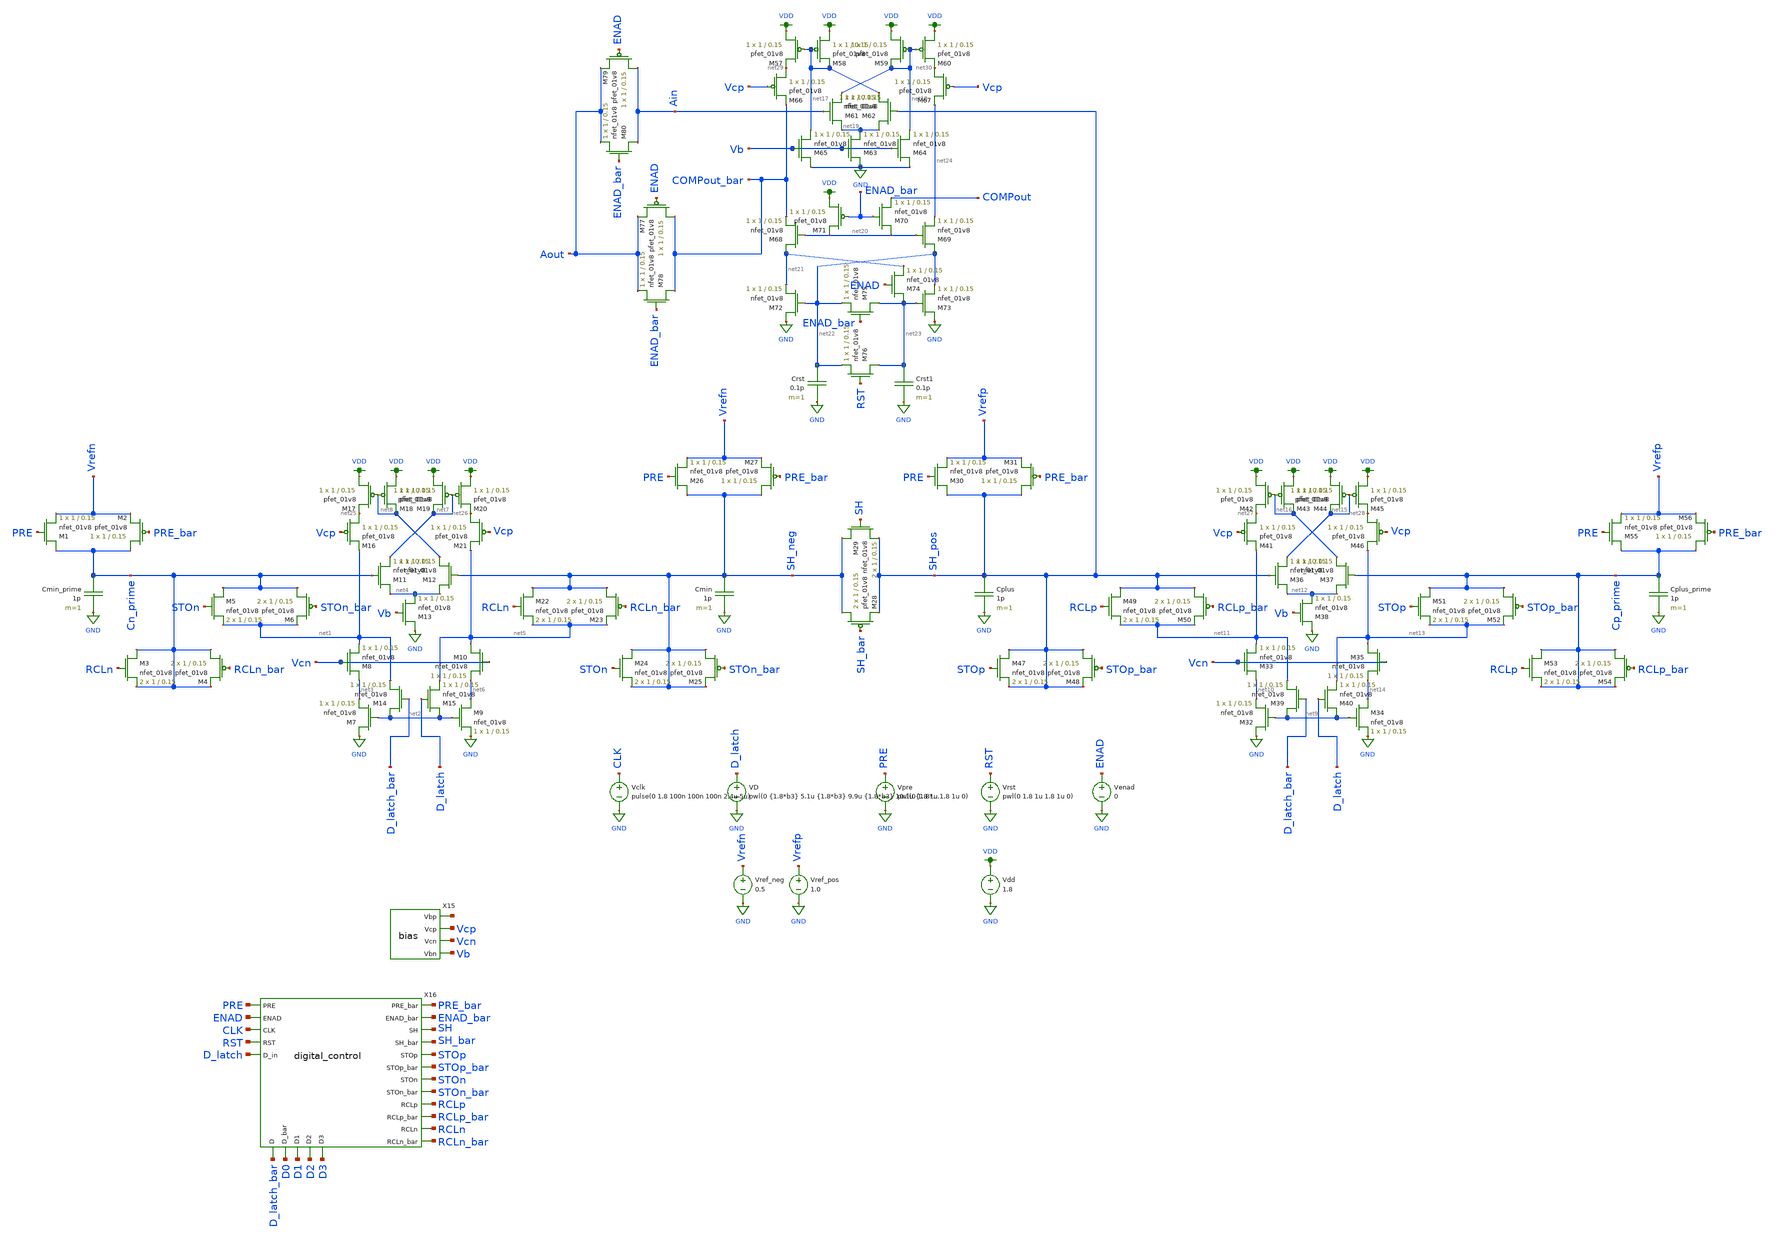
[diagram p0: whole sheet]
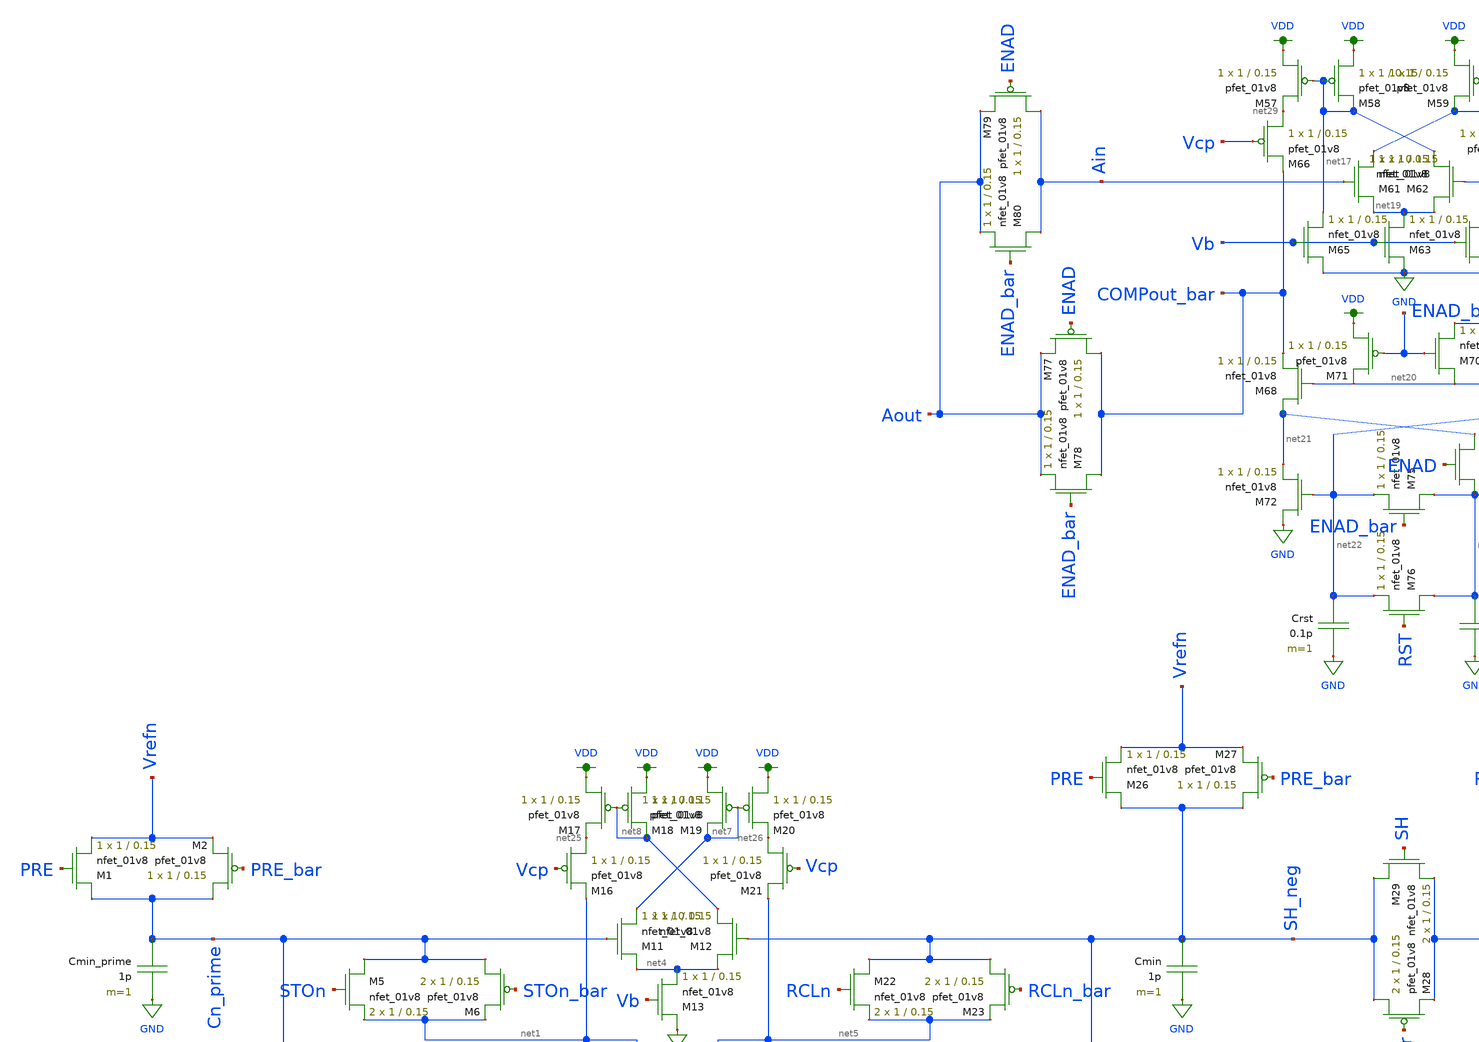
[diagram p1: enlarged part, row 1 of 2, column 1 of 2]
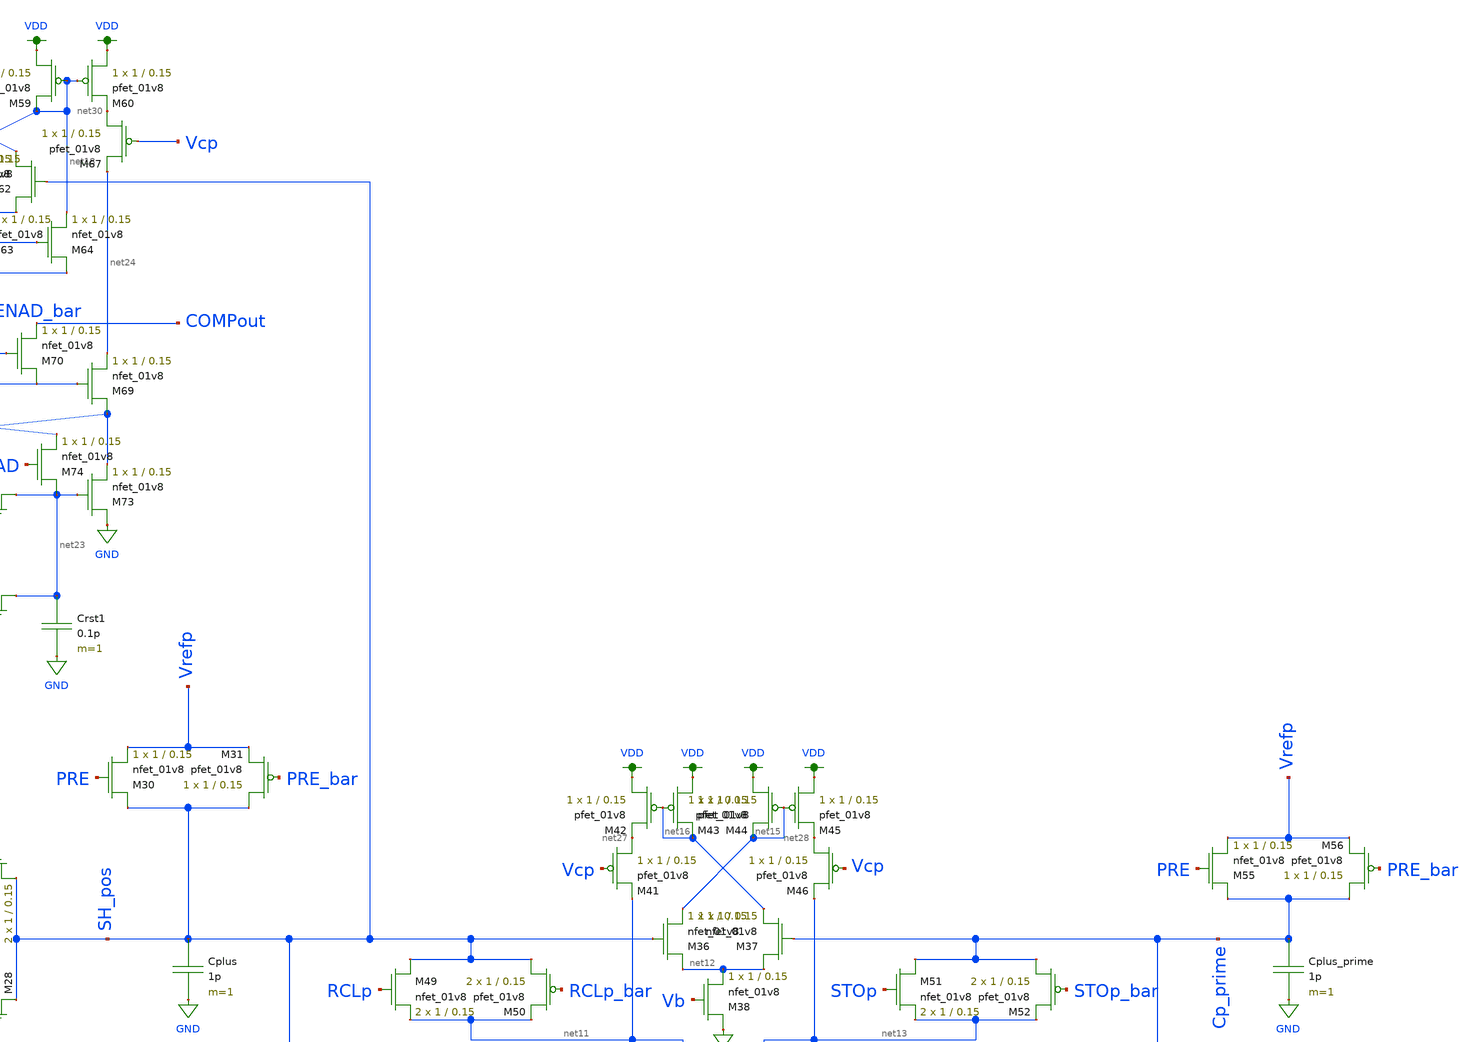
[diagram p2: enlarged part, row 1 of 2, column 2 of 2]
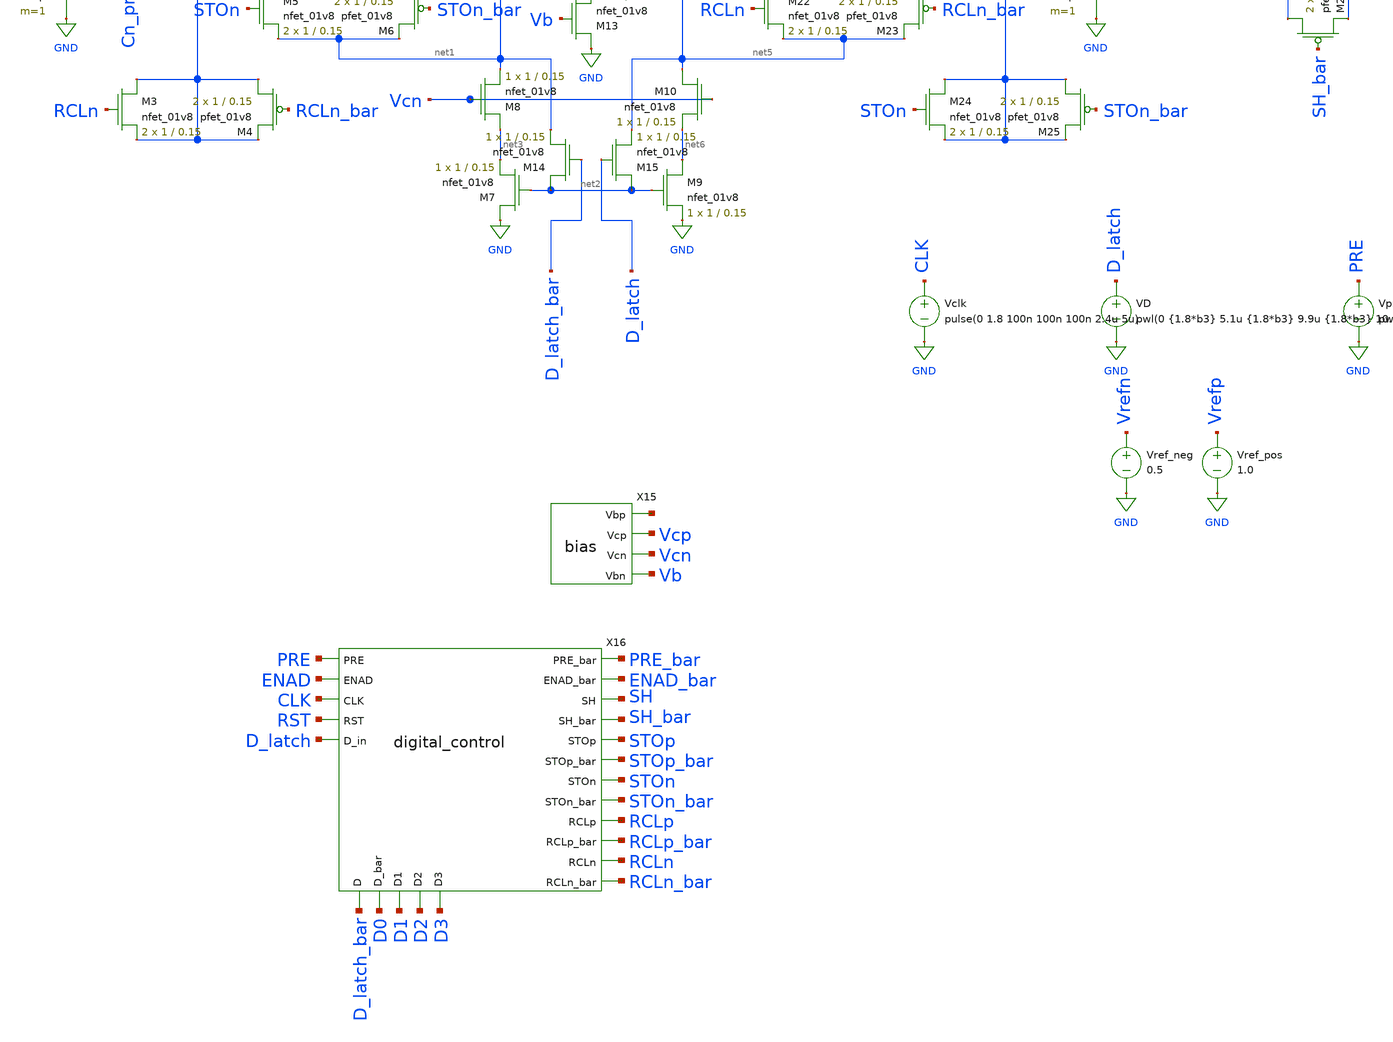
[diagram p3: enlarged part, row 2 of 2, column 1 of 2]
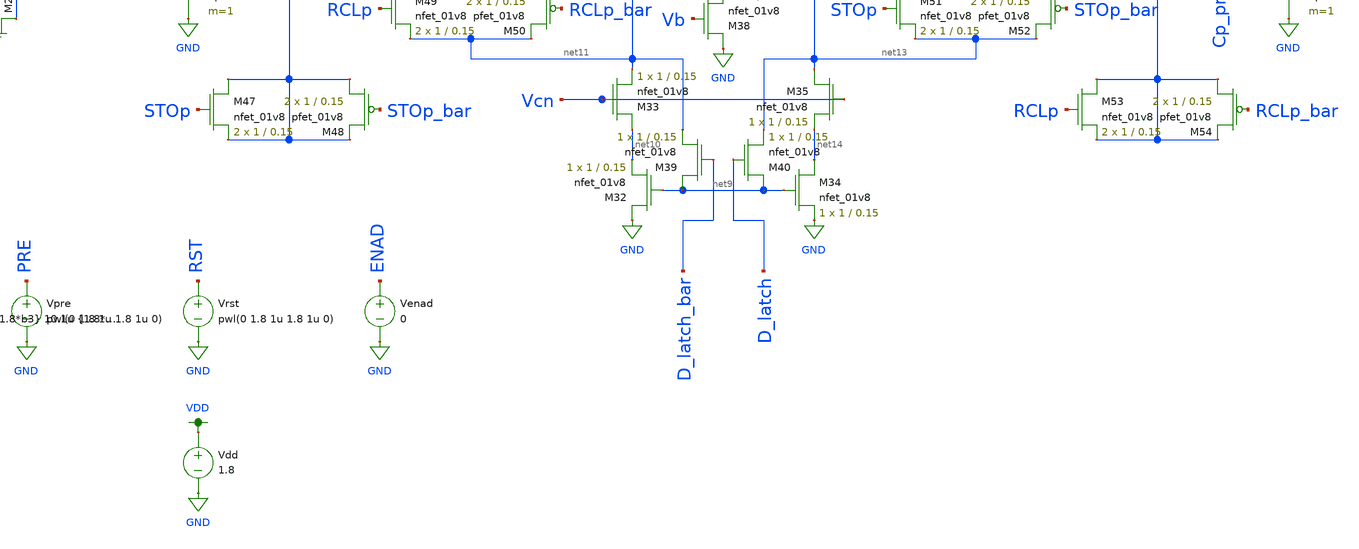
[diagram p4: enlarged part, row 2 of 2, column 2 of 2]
** sch_path: simulations/test_harness_dac.sch
**.subckt test_harness_dac
XM1 Cn_prime PRE Vrefn GND sky130_fd_pr__nfet_01v8 L=0.15 W=1 nf=1 ad='int((nf+1)/2) * W/nf * 0.29' as='int((nf+2)/2) * W/nf * 0.29'
+ pd='2*int((nf+1)/2) * (W/nf + 0.29)' ps='2*int((nf+2)/2) * (W/nf + 0.29)' nrd='0.29 / W' nrs='0.29 / W'
+ sa=0 sb=0 sd=0 mult=1 m=1
XM2 Cn_prime PRE_bar Vrefn VDD sky130_fd_pr__pfet_01v8 L=0.15 W=1 nf=1 ad='int((nf+1)/2) * W/nf * 0.29'
+ as='int((nf+2)/2) * W/nf * 0.29' pd='2*int((nf+1)/2) * (W/nf + 0.29)' ps='2*int((nf+2)/2) * (W/nf + 0.29)'
+ nrd='0.29 / W' nrs='0.29 / W' sa=0 sb=0 sd=0 mult=1 m=1
Cmin_prime Cn_prime GND 1p m=1
XM3 Cn_prime RCLn Cn_prime GND sky130_fd_pr__nfet_01v8 L=0.15 W=1 nf=1 ad='int((nf+1)/2) * W/nf * 0.29'
+ as='int((nf+2)/2) * W/nf * 0.29' pd='2*int((nf+1)/2) * (W/nf + 0.29)' ps='2*int((nf+2)/2) * (W/nf + 0.29)'
+ nrd='0.29 / W' nrs='0.29 / W' sa=0 sb=0 sd=0 mult=2 m=2
XM4 Cn_prime RCLn_bar Cn_prime VDD sky130_fd_pr__pfet_01v8 L=0.15 W=1 nf=1 ad='int((nf+1)/2) * W/nf * 0.29'
+ as='int((nf+2)/2) * W/nf * 0.29' pd='2*int((nf+1)/2) * (W/nf + 0.29)' ps='2*int((nf+2)/2) * (W/nf + 0.29)'
+ nrd='0.29 / W' nrs='0.29 / W' sa=0 sb=0 sd=0 mult=2 m=2
XM5 Cn_prime STOn net1 GND sky130_fd_pr__nfet_01v8 L=0.15 W=1 nf=1 ad='int((nf+1)/2) * W/nf * 0.29' as='int((nf+2)/2) * W/nf * 0.29'
+ pd='2*int((nf+1)/2) * (W/nf + 0.29)' ps='2*int((nf+2)/2) * (W/nf + 0.29)' nrd='0.29 / W' nrs='0.29 / W'
+ sa=0 sb=0 sd=0 mult=2 m=2
XM6 Cn_prime STOn_bar net1 VDD sky130_fd_pr__pfet_01v8 L=0.15 W=1 nf=1 ad='int((nf+1)/2) * W/nf * 0.29'
+ as='int((nf+2)/2) * W/nf * 0.29' pd='2*int((nf+1)/2) * (W/nf + 0.29)' ps='2*int((nf+2)/2) * (W/nf + 0.29)'
+ nrd='0.29 / W' nrs='0.29 / W' sa=0 sb=0 sd=0 mult=2 m=2
XM7 GND net2 net3 GND sky130_fd_pr__nfet_01v8 L=0.15 W=1 nf=1 ad='int((nf+1)/2) * W/nf * 0.29' as='int((nf+2)/2) * W/nf * 0.29'
+ pd='2*int((nf+1)/2) * (W/nf + 0.29)' ps='2*int((nf+2)/2) * (W/nf + 0.29)' nrd='0.29 / W' nrs='0.29 / W'
+ sa=0 sb=0 sd=0 mult=1 m=1
XM8 net3 Vcn net1 GND sky130_fd_pr__nfet_01v8 L=0.15 W=1 nf=1 ad='int((nf+1)/2) * W/nf * 0.29' as='int((nf+2)/2) * W/nf * 0.29'
+ pd='2*int((nf+1)/2) * (W/nf + 0.29)' ps='2*int((nf+2)/2) * (W/nf + 0.29)' nrd='0.29 / W' nrs='0.29 / W'
+ sa=0 sb=0 sd=0 mult=1 m=1
XM9 net6 net2 GND GND sky130_fd_pr__nfet_01v8 L=0.15 W=1 nf=1 ad='int((nf+1)/2) * W/nf * 0.29' as='int((nf+2)/2) * W/nf * 0.29'
+ pd='2*int((nf+1)/2) * (W/nf + 0.29)' ps='2*int((nf+2)/2) * (W/nf + 0.29)' nrd='0.29 / W' nrs='0.29 / W'
+ sa=0 sb=0 sd=0 mult=1 m=1
XM10 net5 Vcn net6 GND sky130_fd_pr__nfet_01v8 L=0.15 W=1 nf=1 ad='int((nf+1)/2) * W/nf * 0.29' as='int((nf+2)/2) * W/nf * 0.29'
+ pd='2*int((nf+1)/2) * (W/nf + 0.29)' ps='2*int((nf+2)/2) * (W/nf + 0.29)' nrd='0.29 / W' nrs='0.29 / W'
+ sa=0 sb=0 sd=0 mult=1 m=1
XM11 net4 Cn_prime net7 GND sky130_fd_pr__nfet_01v8 L=0.15 W=1 nf=1 ad='int((nf+1)/2) * W/nf * 0.29'
+ as='int((nf+2)/2) * W/nf * 0.29' pd='2*int((nf+1)/2) * (W/nf + 0.29)' ps='2*int((nf+2)/2) * (W/nf + 0.29)'
+ nrd='0.29 / W' nrs='0.29 / W' sa=0 sb=0 sd=0 mult=1 m=1
XM12 net4 SH_neg net8 GND sky130_fd_pr__nfet_01v8 L=0.15 W=1 nf=1 ad='int((nf+1)/2) * W/nf * 0.29' as='int((nf+2)/2) * W/nf * 0.29'
+ pd='2*int((nf+1)/2) * (W/nf + 0.29)' ps='2*int((nf+2)/2) * (W/nf + 0.29)' nrd='0.29 / W' nrs='0.29 / W'
+ sa=0 sb=0 sd=0 mult=1 m=1
XM13 GND Vb net4 GND sky130_fd_pr__nfet_01v8 L=0.15 W=1 nf=1 ad='int((nf+1)/2) * W/nf * 0.29' as='int((nf+2)/2) * W/nf * 0.29'
+ pd='2*int((nf+1)/2) * (W/nf + 0.29)' ps='2*int((nf+2)/2) * (W/nf + 0.29)' nrd='0.29 / W' nrs='0.29 / W'
+ sa=0 sb=0 sd=0 mult=1 m=1
XM14 net2 D_latch_bar net1 GND sky130_fd_pr__nfet_01v8 L=0.15 W=1 nf=1 ad='int((nf+1)/2) * W/nf * 0.29'
+ as='int((nf+2)/2) * W/nf * 0.29' pd='2*int((nf+1)/2) * (W/nf + 0.29)' ps='2*int((nf+2)/2) * (W/nf + 0.29)'
+ nrd='0.29 / W' nrs='0.29 / W' sa=0 sb=0 sd=0 mult=1 m=1
XM15 net2 D_latch net5 GND sky130_fd_pr__nfet_01v8 L=0.15 W=1 nf=1 ad='int((nf+1)/2) * W/nf * 0.29' as='int((nf+2)/2) * W/nf * 0.29'
+ pd='2*int((nf+1)/2) * (W/nf + 0.29)' ps='2*int((nf+2)/2) * (W/nf + 0.29)' nrd='0.29 / W' nrs='0.29 / W'
+ sa=0 sb=0 sd=0 mult=1 m=1
XM16 net25 Vcp net1 VDD sky130_fd_pr__pfet_01v8 L=0.15 W=1 nf=1 ad='int((nf+1)/2) * W/nf * 0.29' as='int((nf+2)/2) * W/nf * 0.29'
+ pd='2*int((nf+1)/2) * (W/nf + 0.29)' ps='2*int((nf+2)/2) * (W/nf + 0.29)' nrd='0.29 / W' nrs='0.29 / W'
+ sa=0 sb=0 sd=0 mult=1 m=1
XM17 VDD net8 net25 VDD sky130_fd_pr__pfet_01v8 L=0.15 W=1 nf=1 ad='int((nf+1)/2) * W/nf * 0.29' as='int((nf+2)/2) * W/nf * 0.29'
+ pd='2*int((nf+1)/2) * (W/nf + 0.29)' ps='2*int((nf+2)/2) * (W/nf + 0.29)' nrd='0.29 / W' nrs='0.29 / W'
+ sa=0 sb=0 sd=0 mult=1 m=1
XM18 VDD net8 net8 VDD sky130_fd_pr__pfet_01v8 L=0.15 W=1 nf=1 ad='int((nf+1)/2) * W/nf * 0.29' as='int((nf+2)/2) * W/nf * 0.29'
+ pd='2*int((nf+1)/2) * (W/nf + 0.29)' ps='2*int((nf+2)/2) * (W/nf + 0.29)' nrd='0.29 / W' nrs='0.29 / W'
+ sa=0 sb=0 sd=0 mult=1 m=1
XM19 VDD net7 net7 VDD sky130_fd_pr__pfet_01v8 L=0.15 W=1 nf=1 ad='int((nf+1)/2) * W/nf * 0.29' as='int((nf+2)/2) * W/nf * 0.29'
+ pd='2*int((nf+1)/2) * (W/nf + 0.29)' ps='2*int((nf+2)/2) * (W/nf + 0.29)' nrd='0.29 / W' nrs='0.29 / W'
+ sa=0 sb=0 sd=0 mult=1 m=1
XM20 VDD net7 net26 VDD sky130_fd_pr__pfet_01v8 L=0.15 W=1 nf=1 ad='int((nf+1)/2) * W/nf * 0.29' as='int((nf+2)/2) * W/nf * 0.29'
+ pd='2*int((nf+1)/2) * (W/nf + 0.29)' ps='2*int((nf+2)/2) * (W/nf + 0.29)' nrd='0.29 / W' nrs='0.29 / W'
+ sa=0 sb=0 sd=0 mult=1 m=1
XM21 net26 Vcp net5 VDD sky130_fd_pr__pfet_01v8 L=0.15 W=1 nf=1 ad='int((nf+1)/2) * W/nf * 0.29' as='int((nf+2)/2) * W/nf * 0.29'
+ pd='2*int((nf+1)/2) * (W/nf + 0.29)' ps='2*int((nf+2)/2) * (W/nf + 0.29)' nrd='0.29 / W' nrs='0.29 / W'
+ sa=0 sb=0 sd=0 mult=1 m=1
XM22 SH_neg RCLn net5 GND sky130_fd_pr__nfet_01v8 L=0.15 W=1 nf=1 ad='int((nf+1)/2) * W/nf * 0.29' as='int((nf+2)/2) * W/nf * 0.29'
+ pd='2*int((nf+1)/2) * (W/nf + 0.29)' ps='2*int((nf+2)/2) * (W/nf + 0.29)' nrd='0.29 / W' nrs='0.29 / W'
+ sa=0 sb=0 sd=0 mult=2 m=2
XM23 SH_neg RCLn_bar net5 VDD sky130_fd_pr__pfet_01v8 L=0.15 W=1 nf=1 ad='int((nf+1)/2) * W/nf * 0.29'
+ as='int((nf+2)/2) * W/nf * 0.29' pd='2*int((nf+1)/2) * (W/nf + 0.29)' ps='2*int((nf+2)/2) * (W/nf + 0.29)'
+ nrd='0.29 / W' nrs='0.29 / W' sa=0 sb=0 sd=0 mult=2 m=2
XM24 SH_neg STOn SH_neg GND sky130_fd_pr__nfet_01v8 L=0.15 W=1 nf=1 ad='int((nf+1)/2) * W/nf * 0.29'
+ as='int((nf+2)/2) * W/nf * 0.29' pd='2*int((nf+1)/2) * (W/nf + 0.29)' ps='2*int((nf+2)/2) * (W/nf + 0.29)'
+ nrd='0.29 / W' nrs='0.29 / W' sa=0 sb=0 sd=0 mult=2 m=2
XM25 SH_neg STOn_bar SH_neg VDD sky130_fd_pr__pfet_01v8 L=0.15 W=1 nf=1 ad='int((nf+1)/2) * W/nf * 0.29'
+ as='int((nf+2)/2) * W/nf * 0.29' pd='2*int((nf+1)/2) * (W/nf + 0.29)' ps='2*int((nf+2)/2) * (W/nf + 0.29)'
+ nrd='0.29 / W' nrs='0.29 / W' sa=0 sb=0 sd=0 mult=2 m=2
XM26 SH_neg PRE Vrefn GND sky130_fd_pr__nfet_01v8 L=0.15 W=1 nf=1 ad='int((nf+1)/2) * W/nf * 0.29' as='int((nf+2)/2) * W/nf * 0.29'
+ pd='2*int((nf+1)/2) * (W/nf + 0.29)' ps='2*int((nf+2)/2) * (W/nf + 0.29)' nrd='0.29 / W' nrs='0.29 / W'
+ sa=0 sb=0 sd=0 mult=1 m=1
XM27 SH_neg PRE_bar Vrefn VDD sky130_fd_pr__pfet_01v8 L=0.15 W=1 nf=1 ad='int((nf+1)/2) * W/nf * 0.29'
+ as='int((nf+2)/2) * W/nf * 0.29' pd='2*int((nf+1)/2) * (W/nf + 0.29)' ps='2*int((nf+2)/2) * (W/nf + 0.29)'
+ nrd='0.29 / W' nrs='0.29 / W' sa=0 sb=0 sd=0 mult=1 m=1
Cmin SH_neg GND 1p m=1
XM28 SH_neg SH_bar SH_pos VDD sky130_fd_pr__pfet_01v8 L=0.15 W=1 nf=1 ad='int((nf+1)/2) * W/nf * 0.29'
+ as='int((nf+2)/2) * W/nf * 0.29' pd='2*int((nf+1)/2) * (W/nf + 0.29)' ps='2*int((nf+2)/2) * (W/nf + 0.29)'
+ nrd='0.29 / W' nrs='0.29 / W' sa=0 sb=0 sd=0 mult=2 m=2
XM29 SH_neg SH SH_pos GND sky130_fd_pr__nfet_01v8 L=0.15 W=1 nf=1 ad='int((nf+1)/2) * W/nf * 0.29' as='int((nf+2)/2) * W/nf * 0.29'
+ pd='2*int((nf+1)/2) * (W/nf + 0.29)' ps='2*int((nf+2)/2) * (W/nf + 0.29)' nrd='0.29 / W' nrs='0.29 / W'
+ sa=0 sb=0 sd=0 mult=2 m=2
XM30 SH_pos PRE Vrefp GND sky130_fd_pr__nfet_01v8 L=0.15 W=1 nf=1 ad='int((nf+1)/2) * W/nf * 0.29' as='int((nf+2)/2) * W/nf * 0.29'
+ pd='2*int((nf+1)/2) * (W/nf + 0.29)' ps='2*int((nf+2)/2) * (W/nf + 0.29)' nrd='0.29 / W' nrs='0.29 / W'
+ sa=0 sb=0 sd=0 mult=1 m=1
XM31 SH_pos PRE_bar Vrefp VDD sky130_fd_pr__pfet_01v8 L=0.15 W=1 nf=1 ad='int((nf+1)/2) * W/nf * 0.29'
+ as='int((nf+2)/2) * W/nf * 0.29' pd='2*int((nf+1)/2) * (W/nf + 0.29)' ps='2*int((nf+2)/2) * (W/nf + 0.29)'
+ nrd='0.29 / W' nrs='0.29 / W' sa=0 sb=0 sd=0 mult=1 m=1
Cplus SH_pos GND 1p m=1
XM32 GND net9 net10 GND sky130_fd_pr__nfet_01v8 L=0.15 W=1 nf=1 ad='int((nf+1)/2) * W/nf * 0.29' as='int((nf+2)/2) * W/nf * 0.29'
+ pd='2*int((nf+1)/2) * (W/nf + 0.29)' ps='2*int((nf+2)/2) * (W/nf + 0.29)' nrd='0.29 / W' nrs='0.29 / W'
+ sa=0 sb=0 sd=0 mult=1 m=1
XM33 net10 Vcn net11 GND sky130_fd_pr__nfet_01v8 L=0.15 W=1 nf=1 ad='int((nf+1)/2) * W/nf * 0.29' as='int((nf+2)/2) * W/nf * 0.29'
+ pd='2*int((nf+1)/2) * (W/nf + 0.29)' ps='2*int((nf+2)/2) * (W/nf + 0.29)' nrd='0.29 / W' nrs='0.29 / W'
+ sa=0 sb=0 sd=0 mult=1 m=1
XM34 net14 net9 GND GND sky130_fd_pr__nfet_01v8 L=0.15 W=1 nf=1 ad='int((nf+1)/2) * W/nf * 0.29' as='int((nf+2)/2) * W/nf * 0.29'
+ pd='2*int((nf+1)/2) * (W/nf + 0.29)' ps='2*int((nf+2)/2) * (W/nf + 0.29)' nrd='0.29 / W' nrs='0.29 / W'
+ sa=0 sb=0 sd=0 mult=1 m=1
XM35 net13 Vcn net14 GND sky130_fd_pr__nfet_01v8 L=0.15 W=1 nf=1 ad='int((nf+1)/2) * W/nf * 0.29' as='int((nf+2)/2) * W/nf * 0.29'
+ pd='2*int((nf+1)/2) * (W/nf + 0.29)' ps='2*int((nf+2)/2) * (W/nf + 0.29)' nrd='0.29 / W' nrs='0.29 / W'
+ sa=0 sb=0 sd=0 mult=1 m=1
XM36 net12 SH_pos net15 GND sky130_fd_pr__nfet_01v8 L=0.15 W=1 nf=1 ad='int((nf+1)/2) * W/nf * 0.29'
+ as='int((nf+2)/2) * W/nf * 0.29' pd='2*int((nf+1)/2) * (W/nf + 0.29)' ps='2*int((nf+2)/2) * (W/nf + 0.29)'
+ nrd='0.29 / W' nrs='0.29 / W' sa=0 sb=0 sd=0 mult=1 m=1
XM37 net12 Cp_prime net16 GND sky130_fd_pr__nfet_01v8 L=0.15 W=1 nf=1 ad='int((nf+1)/2) * W/nf * 0.29'
+ as='int((nf+2)/2) * W/nf * 0.29' pd='2*int((nf+1)/2) * (W/nf + 0.29)' ps='2*int((nf+2)/2) * (W/nf + 0.29)'
+ nrd='0.29 / W' nrs='0.29 / W' sa=0 sb=0 sd=0 mult=1 m=1
XM38 GND Vb net12 GND sky130_fd_pr__nfet_01v8 L=0.15 W=1 nf=1 ad='int((nf+1)/2) * W/nf * 0.29' as='int((nf+2)/2) * W/nf * 0.29'
+ pd='2*int((nf+1)/2) * (W/nf + 0.29)' ps='2*int((nf+2)/2) * (W/nf + 0.29)' nrd='0.29 / W' nrs='0.29 / W'
+ sa=0 sb=0 sd=0 mult=1 m=1
XM39 net9 D_latch_bar net11 GND sky130_fd_pr__nfet_01v8 L=0.15 W=1 nf=1 ad='int((nf+1)/2) * W/nf * 0.29'
+ as='int((nf+2)/2) * W/nf * 0.29' pd='2*int((nf+1)/2) * (W/nf + 0.29)' ps='2*int((nf+2)/2) * (W/nf + 0.29)'
+ nrd='0.29 / W' nrs='0.29 / W' sa=0 sb=0 sd=0 mult=1 m=1
XM40 net9 D_latch net13 GND sky130_fd_pr__nfet_01v8 L=0.15 W=1 nf=1 ad='int((nf+1)/2) * W/nf * 0.29'
+ as='int((nf+2)/2) * W/nf * 0.29' pd='2*int((nf+1)/2) * (W/nf + 0.29)' ps='2*int((nf+2)/2) * (W/nf + 0.29)'
+ nrd='0.29 / W' nrs='0.29 / W' sa=0 sb=0 sd=0 mult=1 m=1
XM41 net27 Vcp net11 VDD sky130_fd_pr__pfet_01v8 L=0.15 W=1 nf=1 ad='int((nf+1)/2) * W/nf * 0.29' as='int((nf+2)/2) * W/nf * 0.29'
+ pd='2*int((nf+1)/2) * (W/nf + 0.29)' ps='2*int((nf+2)/2) * (W/nf + 0.29)' nrd='0.29 / W' nrs='0.29 / W'
+ sa=0 sb=0 sd=0 mult=1 m=1
XM42 VDD net16 net27 VDD sky130_fd_pr__pfet_01v8 L=0.15 W=1 nf=1 ad='int((nf+1)/2) * W/nf * 0.29' as='int((nf+2)/2) * W/nf * 0.29'
+ pd='2*int((nf+1)/2) * (W/nf + 0.29)' ps='2*int((nf+2)/2) * (W/nf + 0.29)' nrd='0.29 / W' nrs='0.29 / W'
+ sa=0 sb=0 sd=0 mult=1 m=1
XM43 VDD net16 net16 VDD sky130_fd_pr__pfet_01v8 L=0.15 W=1 nf=1 ad='int((nf+1)/2) * W/nf * 0.29' as='int((nf+2)/2) * W/nf * 0.29'
+ pd='2*int((nf+1)/2) * (W/nf + 0.29)' ps='2*int((nf+2)/2) * (W/nf + 0.29)' nrd='0.29 / W' nrs='0.29 / W'
+ sa=0 sb=0 sd=0 mult=1 m=1
XM44 VDD net15 net15 VDD sky130_fd_pr__pfet_01v8 L=0.15 W=1 nf=1 ad='int((nf+1)/2) * W/nf * 0.29' as='int((nf+2)/2) * W/nf * 0.29'
+ pd='2*int((nf+1)/2) * (W/nf + 0.29)' ps='2*int((nf+2)/2) * (W/nf + 0.29)' nrd='0.29 / W' nrs='0.29 / W'
+ sa=0 sb=0 sd=0 mult=1 m=1
XM45 VDD net15 net28 VDD sky130_fd_pr__pfet_01v8 L=0.15 W=1 nf=1 ad='int((nf+1)/2) * W/nf * 0.29' as='int((nf+2)/2) * W/nf * 0.29'
+ pd='2*int((nf+1)/2) * (W/nf + 0.29)' ps='2*int((nf+2)/2) * (W/nf + 0.29)' nrd='0.29 / W' nrs='0.29 / W'
+ sa=0 sb=0 sd=0 mult=1 m=1
XM46 net28 Vcp net13 VDD sky130_fd_pr__pfet_01v8 L=0.15 W=1 nf=1 ad='int((nf+1)/2) * W/nf * 0.29' as='int((nf+2)/2) * W/nf * 0.29'
+ pd='2*int((nf+1)/2) * (W/nf + 0.29)' ps='2*int((nf+2)/2) * (W/nf + 0.29)' nrd='0.29 / W' nrs='0.29 / W'
+ sa=0 sb=0 sd=0 mult=1 m=1
XM47 SH_pos STOp SH_pos GND sky130_fd_pr__nfet_01v8 L=0.15 W=1 nf=1 ad='int((nf+1)/2) * W/nf * 0.29'
+ as='int((nf+2)/2) * W/nf * 0.29' pd='2*int((nf+1)/2) * (W/nf + 0.29)' ps='2*int((nf+2)/2) * (W/nf + 0.29)'
+ nrd='0.29 / W' nrs='0.29 / W' sa=0 sb=0 sd=0 mult=2 m=2
XM48 SH_pos STOp_bar SH_pos VDD sky130_fd_pr__pfet_01v8 L=0.15 W=1 nf=1 ad='int((nf+1)/2) * W/nf * 0.29'
+ as='int((nf+2)/2) * W/nf * 0.29' pd='2*int((nf+1)/2) * (W/nf + 0.29)' ps='2*int((nf+2)/2) * (W/nf + 0.29)'
+ nrd='0.29 / W' nrs='0.29 / W' sa=0 sb=0 sd=0 mult=2 m=2
XM49 SH_pos RCLp net11 GND sky130_fd_pr__nfet_01v8 L=0.15 W=1 nf=1 ad='int((nf+1)/2) * W/nf * 0.29' as='int((nf+2)/2) * W/nf * 0.29'
+ pd='2*int((nf+1)/2) * (W/nf + 0.29)' ps='2*int((nf+2)/2) * (W/nf + 0.29)' nrd='0.29 / W' nrs='0.29 / W'
+ sa=0 sb=0 sd=0 mult=2 m=2
XM50 SH_pos RCLp_bar net11 VDD sky130_fd_pr__pfet_01v8 L=0.15 W=1 nf=1 ad='int((nf+1)/2) * W/nf * 0.29'
+ as='int((nf+2)/2) * W/nf * 0.29' pd='2*int((nf+1)/2) * (W/nf + 0.29)' ps='2*int((nf+2)/2) * (W/nf + 0.29)'
+ nrd='0.29 / W' nrs='0.29 / W' sa=0 sb=0 sd=0 mult=2 m=2
XM51 Cp_prime STOp net13 GND sky130_fd_pr__nfet_01v8 L=0.15 W=1 nf=1 ad='int((nf+1)/2) * W/nf * 0.29'
+ as='int((nf+2)/2) * W/nf * 0.29' pd='2*int((nf+1)/2) * (W/nf + 0.29)' ps='2*int((nf+2)/2) * (W/nf + 0.29)'
+ nrd='0.29 / W' nrs='0.29 / W' sa=0 sb=0 sd=0 mult=2 m=2
XM52 Cp_prime STOp_bar net13 VDD sky130_fd_pr__pfet_01v8 L=0.15 W=1 nf=1 ad='int((nf+1)/2) * W/nf * 0.29'
+ as='int((nf+2)/2) * W/nf * 0.29' pd='2*int((nf+1)/2) * (W/nf + 0.29)' ps='2*int((nf+2)/2) * (W/nf + 0.29)'
+ nrd='0.29 / W' nrs='0.29 / W' sa=0 sb=0 sd=0 mult=2 m=2
XM53 Cp_prime RCLp Cp_prime GND sky130_fd_pr__nfet_01v8 L=0.15 W=1 nf=1 ad='int((nf+1)/2) * W/nf * 0.29'
+ as='int((nf+2)/2) * W/nf * 0.29' pd='2*int((nf+1)/2) * (W/nf + 0.29)' ps='2*int((nf+2)/2) * (W/nf + 0.29)'
+ nrd='0.29 / W' nrs='0.29 / W' sa=0 sb=0 sd=0 mult=2 m=2
XM54 Cp_prime RCLp_bar Cp_prime VDD sky130_fd_pr__pfet_01v8 L=0.15 W=1 nf=1 ad='int((nf+1)/2) * W/nf * 0.29'
+ as='int((nf+2)/2) * W/nf * 0.29' pd='2*int((nf+1)/2) * (W/nf + 0.29)' ps='2*int((nf+2)/2) * (W/nf + 0.29)'
+ nrd='0.29 / W' nrs='0.29 / W' sa=0 sb=0 sd=0 mult=2 m=2
XM55 Cp_prime PRE Vrefp GND sky130_fd_pr__nfet_01v8 L=0.15 W=1 nf=1 ad='int((nf+1)/2) * W/nf * 0.29'
+ as='int((nf+2)/2) * W/nf * 0.29' pd='2*int((nf+1)/2) * (W/nf + 0.29)' ps='2*int((nf+2)/2) * (W/nf + 0.29)'
+ nrd='0.29 / W' nrs='0.29 / W' sa=0 sb=0 sd=0 mult=1 m=1
XM56 Cp_prime PRE_bar Vrefp VDD sky130_fd_pr__pfet_01v8 L=0.15 W=1 nf=1 ad='int((nf+1)/2) * W/nf * 0.29'
+ as='int((nf+2)/2) * W/nf * 0.29' pd='2*int((nf+1)/2) * (W/nf + 0.29)' ps='2*int((nf+2)/2) * (W/nf + 0.29)'
+ nrd='0.29 / W' nrs='0.29 / W' sa=0 sb=0 sd=0 mult=1 m=1
Cplus_prime Cp_prime GND 1p m=1
XM57 VDD net17 net29 VDD sky130_fd_pr__pfet_01v8 L=0.15 W=1 nf=1 ad='int((nf+1)/2) * W/nf * 0.29' as='int((nf+2)/2) * W/nf * 0.29'
+ pd='2*int((nf+1)/2) * (W/nf + 0.29)' ps='2*int((nf+2)/2) * (W/nf + 0.29)' nrd='0.29 / W' nrs='0.29 / W'
+ sa=0 sb=0 sd=0 mult=1 m=1
XM58 VDD net17 net17 VDD sky130_fd_pr__pfet_01v8 L=0.15 W=1 nf=1 ad='int((nf+1)/2) * W/nf * 0.29' as='int((nf+2)/2) * W/nf * 0.29'
+ pd='2*int((nf+1)/2) * (W/nf + 0.29)' ps='2*int((nf+2)/2) * (W/nf + 0.29)' nrd='0.29 / W' nrs='0.29 / W'
+ sa=0 sb=0 sd=0 mult=1 m=1
XM59 VDD net18 net18 VDD sky130_fd_pr__pfet_01v8 L=0.15 W=1 nf=1 ad='int((nf+1)/2) * W/nf * 0.29' as='int((nf+2)/2) * W/nf * 0.29'
+ pd='2*int((nf+1)/2) * (W/nf + 0.29)' ps='2*int((nf+2)/2) * (W/nf + 0.29)' nrd='0.29 / W' nrs='0.29 / W'
+ sa=0 sb=0 sd=0 mult=1 m=1
XM60 VDD net18 net30 VDD sky130_fd_pr__pfet_01v8 L=0.15 W=1 nf=1 ad='int((nf+1)/2) * W/nf * 0.29' as='int((nf+2)/2) * W/nf * 0.29'
+ pd='2*int((nf+1)/2) * (W/nf + 0.29)' ps='2*int((nf+2)/2) * (W/nf + 0.29)' nrd='0.29 / W' nrs='0.29 / W'
+ sa=0 sb=0 sd=0 mult=1 m=1
XM61 net19 Ain net18 GND sky130_fd_pr__nfet_01v8 L=0.15 W=1 nf=1 ad='int((nf+1)/2) * W/nf * 0.29' as='int((nf+2)/2) * W/nf * 0.29'
+ pd='2*int((nf+1)/2) * (W/nf + 0.29)' ps='2*int((nf+2)/2) * (W/nf + 0.29)' nrd='0.29 / W' nrs='0.29 / W'
+ sa=0 sb=0 sd=0 mult=1 m=1
XM62 net19 SH_pos net17 GND sky130_fd_pr__nfet_01v8 L=0.15 W=1 nf=1 ad='int((nf+1)/2) * W/nf * 0.29'
+ as='int((nf+2)/2) * W/nf * 0.29' pd='2*int((nf+1)/2) * (W/nf + 0.29)' ps='2*int((nf+2)/2) * (W/nf + 0.29)'
+ nrd='0.29 / W' nrs='0.29 / W' sa=0 sb=0 sd=0 mult=1 m=1
XM63 GND Vb net19 GND sky130_fd_pr__nfet_01v8 L=0.15 W=1 nf=1 ad='int((nf+1)/2) * W/nf * 0.29' as='int((nf+2)/2) * W/nf * 0.29'
+ pd='2*int((nf+1)/2) * (W/nf + 0.29)' ps='2*int((nf+2)/2) * (W/nf + 0.29)' nrd='0.29 / W' nrs='0.29 / W'
+ sa=0 sb=0 sd=0 mult=1 m=1
XM64 GND Vb net18 GND sky130_fd_pr__nfet_01v8 L=0.15 W=1 nf=1 ad='int((nf+1)/2) * W/nf * 0.29' as='int((nf+2)/2) * W/nf * 0.29'
+ pd='2*int((nf+1)/2) * (W/nf + 0.29)' ps='2*int((nf+2)/2) * (W/nf + 0.29)' nrd='0.29 / W' nrs='0.29 / W'
+ sa=0 sb=0 sd=0 mult=1 m=1
XM65 GND Vb net17 GND sky130_fd_pr__nfet_01v8 L=0.15 W=1 nf=1 ad='int((nf+1)/2) * W/nf * 0.29' as='int((nf+2)/2) * W/nf * 0.29'
+ pd='2*int((nf+1)/2) * (W/nf + 0.29)' ps='2*int((nf+2)/2) * (W/nf + 0.29)' nrd='0.29 / W' nrs='0.29 / W'
+ sa=0 sb=0 sd=0 mult=1 m=1
XM66 net29 Vcp COMPout_bar VDD sky130_fd_pr__pfet_01v8 L=0.15 W=1 nf=1 ad='int((nf+1)/2) * W/nf * 0.29'
+ as='int((nf+2)/2) * W/nf * 0.29' pd='2*int((nf+1)/2) * (W/nf + 0.29)' ps='2*int((nf+2)/2) * (W/nf + 0.29)'
+ nrd='0.29 / W' nrs='0.29 / W' sa=0 sb=0 sd=0 mult=1 m=1
XM67 net30 Vcp net24 VDD sky130_fd_pr__pfet_01v8 L=0.15 W=1 nf=1 ad='int((nf+1)/2) * W/nf * 0.29' as='int((nf+2)/2) * W/nf * 0.29'
+ pd='2*int((nf+1)/2) * (W/nf + 0.29)' ps='2*int((nf+2)/2) * (W/nf + 0.29)' nrd='0.29 / W' nrs='0.29 / W'
+ sa=0 sb=0 sd=0 mult=1 m=1
XM68 net21 net20 COMPout_bar GND sky130_fd_pr__nfet_01v8 L=0.15 W=1 nf=1 ad='int((nf+1)/2) * W/nf * 0.29'
+ as='int((nf+2)/2) * W/nf * 0.29' pd='2*int((nf+1)/2) * (W/nf + 0.29)' ps='2*int((nf+2)/2) * (W/nf + 0.29)'
+ nrd='0.29 / W' nrs='0.29 / W' sa=0 sb=0 sd=0 mult=1 m=1
XM69 net22 net20 net24 GND sky130_fd_pr__nfet_01v8 L=0.15 W=1 nf=1 ad='int((nf+1)/2) * W/nf * 0.29' as='int((nf+2)/2) * W/nf * 0.29'
+ pd='2*int((nf+1)/2) * (W/nf + 0.29)' ps='2*int((nf+2)/2) * (W/nf + 0.29)' nrd='0.29 / W' nrs='0.29 / W'
+ sa=0 sb=0 sd=0 mult=1 m=1
XM70 net20 ENAD_bar COMPout GND sky130_fd_pr__nfet_01v8 L=0.15 W=1 nf=1 ad='int((nf+1)/2) * W/nf * 0.29'
+ as='int((nf+2)/2) * W/nf * 0.29' pd='2*int((nf+1)/2) * (W/nf + 0.29)' ps='2*int((nf+2)/2) * (W/nf + 0.29)'
+ nrd='0.29 / W' nrs='0.29 / W' sa=0 sb=0 sd=0 mult=1 m=1
XM71 VDD ENAD_bar net20 VDD sky130_fd_pr__pfet_01v8 L=0.15 W=1 nf=1 ad='int((nf+1)/2) * W/nf * 0.29'
+ as='int((nf+2)/2) * W/nf * 0.29' pd='2*int((nf+1)/2) * (W/nf + 0.29)' ps='2*int((nf+2)/2) * (W/nf + 0.29)'
+ nrd='0.29 / W' nrs='0.29 / W' sa=0 sb=0 sd=0 mult=1 m=1
XM72 GND net22 net21 GND sky130_fd_pr__nfet_01v8 L=0.15 W=1 nf=1 ad='int((nf+1)/2) * W/nf * 0.29' as='int((nf+2)/2) * W/nf * 0.29'
+ pd='2*int((nf+1)/2) * (W/nf + 0.29)' ps='2*int((nf+2)/2) * (W/nf + 0.29)' nrd='0.29 / W' nrs='0.29 / W'
+ sa=0 sb=0 sd=0 mult=1 m=1
XM73 GND net23 net22 GND sky130_fd_pr__nfet_01v8 L=0.15 W=1 nf=1 ad='int((nf+1)/2) * W/nf * 0.29' as='int((nf+2)/2) * W/nf * 0.29'
+ pd='2*int((nf+1)/2) * (W/nf + 0.29)' ps='2*int((nf+2)/2) * (W/nf + 0.29)' nrd='0.29 / W' nrs='0.29 / W'
+ sa=0 sb=0 sd=0 mult=1 m=1
XM74 net23 ENAD net21 GND sky130_fd_pr__nfet_01v8 L=0.15 W=1 nf=1 ad='int((nf+1)/2) * W/nf * 0.29' as='int((nf+2)/2) * W/nf * 0.29'
+ pd='2*int((nf+1)/2) * (W/nf + 0.29)' ps='2*int((nf+2)/2) * (W/nf + 0.29)' nrd='0.29 / W' nrs='0.29 / W'
+ sa=0 sb=0 sd=0 mult=1 m=1
XM75 net23 ENAD_bar net22 GND sky130_fd_pr__nfet_01v8 L=0.15 W=1 nf=1 ad='int((nf+1)/2) * W/nf * 0.29'
+ as='int((nf+2)/2) * W/nf * 0.29' pd='2*int((nf+1)/2) * (W/nf + 0.29)' ps='2*int((nf+2)/2) * (W/nf + 0.29)'
+ nrd='0.29 / W' nrs='0.29 / W' sa=0 sb=0 sd=0 mult=1 m=1
Crst net22 GND 0.1p m=1
XM76 net23 RST net22 GND sky130_fd_pr__nfet_01v8 L=0.15 W=1 nf=1 ad='int((nf+1)/2) * W/nf * 0.29' as='int((nf+2)/2) * W/nf * 0.29'
+ pd='2*int((nf+1)/2) * (W/nf + 0.29)' ps='2*int((nf+2)/2) * (W/nf + 0.29)' nrd='0.29 / W' nrs='0.29 / W'
+ sa=0 sb=0 sd=0 mult=1 m=1
Crst1 net23 GND 0.1p m=1
XM77 COMPout_bar ENAD Aout VDD sky130_fd_pr__pfet_01v8 L=0.15 W=1 nf=1 ad='int((nf+1)/2) * W/nf * 0.29'
+ as='int((nf+2)/2) * W/nf * 0.29' pd='2*int((nf+1)/2) * (W/nf + 0.29)' ps='2*int((nf+2)/2) * (W/nf + 0.29)'
+ nrd='0.29 / W' nrs='0.29 / W' sa=0 sb=0 sd=0 mult=1 m=1
XM78 COMPout_bar ENAD_bar Aout GND sky130_fd_pr__nfet_01v8 L=0.15 W=1 nf=1 ad='int((nf+1)/2) * W/nf * 0.29'
+ as='int((nf+2)/2) * W/nf * 0.29' pd='2*int((nf+1)/2) * (W/nf + 0.29)' ps='2*int((nf+2)/2) * (W/nf + 0.29)'
+ nrd='0.29 / W' nrs='0.29 / W' sa=0 sb=0 sd=0 mult=1 m=1
Vclk CLK GND pulse(0 1.8 100n 100n 100n 2.4u 5u)
Vpre PRE GND pwl(0 1.8 1u 1.8 1u 0)
Vrst RST GND pwl(0 1.8 1u 1.8 1u 0)
Venad ENAD GND 0
X15 net31 Vcp Vcn Vb bias
XM79 Ain ENAD Aout VDD sky130_fd_pr__pfet_01v8 L=0.15 W=1 nf=1 ad='int((nf+1)/2) * W/nf * 0.29' as='int((nf+2)/2) * W/nf * 0.29'
+ pd='2*int((nf+1)/2) * (W/nf + 0.29)' ps='2*int((nf+2)/2) * (W/nf + 0.29)' nrd='0.29 / W' nrs='0.29 / W'
+ sa=0 sb=0 sd=0 mult=1 m=1
XM80 Ain ENAD_bar Aout GND sky130_fd_pr__nfet_01v8 L=0.15 W=1 nf=1 ad='int((nf+1)/2) * W/nf * 0.29' as='int((nf+2)/2) * W/nf * 0.29'
+ pd='2*int((nf+1)/2) * (W/nf + 0.29)' ps='2*int((nf+2)/2) * (W/nf + 0.29)' nrd='0.29 / W' nrs='0.29 / W'
+ sa=0 sb=0 sd=0 mult=1 m=1
Vref_neg Vrefn GND 0.5
Vref_pos Vrefp GND 1.0
Vdd VDD GND 1.8
X16 STOn RCLn SH STOp RCLp SH_bar ENAD_bar PRE_bar PRE ENAD D_latch_bar D0 CLK STOp_bar STOn_bar
+ RCLp_bar RCLn_bar D1 D2 D3 RST D_latch digital_control
VD D_latch GND pwl(0 {1.8*b3} 5.1u {1.8*b3} 9.9u {1.8*b3} 10.1u {1.8*b2} 14.9u {1.8*b2} 15.1u {1.8*b1}
+ 19.9u {1.8*b1} 20.1u {1.8*b0} 44.9u {1.8*b0})
**** begin user architecture code

.option wnflag=1
.param MC_SWITCH=0.0
.lib ~/skywater/skywater-pdk/libraries/sky130_fd_pr_ngspice/latest/models/sky130.lib.spice tt



.ic v(D_latch)=0 v(D2)=0 v(D1)=0 v(D0)=0
.ic v(D_latch_bar)=1.8 v(x16.D2_bar)=1.8 v(x16.D1_bar)=1.8 v(x16.D0_bar)=1.8
.param b3 = 1
.param b2 = 1
.param b1 = 0
.param b0 = 1
.control
  set wr_vecnames
  set wr_singlescale
  let code = 0
  while code < 16
    if code eq 0
      alterparam b0 = 0
    else
      alterparam b0 = code % 2
    end
    if floor(code / 2) eq 0
      alterparam b1 = 0
    else
      alterparam b1 = floor(code / 2) % 2
    end
    if floor(code / 4) eq 0
      alterparam b2 = 0
    else
      alterparam b2 = floor(code / 4) % 2
    end
    if floor(code / 8) eq 0
      alterparam b3 = 0
    else
      alterparam b3 = floor(code / 8) % 2
    end
    save all
    tran 10n 24u
    wrdata ~/Documents/algorithmic-ada-converter/python/dac/dac.txt v(D_latch) v(Aout)
    if code eq 0
      set appendwrite
      set wr_vecnames = FALSE
    end
    let code = code + 1
  end
.endc

**** end user architecture code
**.ends

* expanding   symbol:  ../schematics/bias.sym # of pins=4
** sym_path: schematics/bias.sym
** sch_path: schematics/bias.sch
.subckt bias Vbp Vcp Vcn Vbn
*.opin Vcp
*.opin Vcn
*.opin Vbn
*.opin Vbp
XM1 net1 Vbn GND GND sky130_fd_pr__nfet_01v8 L=2.5 W=12 nf=1 ad='int((nf+1)/2) * W/nf * 0.29' as='int((nf+2)/2) * W/nf * 0.29'
+ pd='2*int((nf+1)/2) * (W/nf + 0.29)' ps='2*int((nf+2)/2) * (W/nf + 0.29)' nrd='0.29 / W' nrs='0.29 / W'
+ sa=0 sb=0 sd=0 mult=1 m=1
XM2 Vcp Vbn GND GND sky130_fd_pr__nfet_01v8 L=0.5 W=12 nf=1 ad='int((nf+1)/2) * W/nf * 0.29' as='int((nf+2)/2) * W/nf * 0.29'
+ pd='2*int((nf+1)/2) * (W/nf + 0.29)' ps='2*int((nf+2)/2) * (W/nf + 0.29)' nrd='0.29 / W' nrs='0.29 / W'
+ sa=0 sb=0 sd=0 mult=1 m=1
XM3 Vbp Vbn GND GND sky130_fd_pr__nfet_01v8 L=0.5 W=12 nf=1 ad='int((nf+1)/2) * W/nf * 0.29' as='int((nf+2)/2) * W/nf * 0.29'
+ pd='2*int((nf+1)/2) * (W/nf + 0.29)' ps='2*int((nf+2)/2) * (W/nf + 0.29)' nrd='0.29 / W' nrs='0.29 / W'
+ sa=0 sb=0 sd=0 mult=1 m=1
XM4 net3 net4 GND GND sky130_fd_pr__nfet_01v8 L=0.5 W=12 nf=1 ad='int((nf+1)/2) * W/nf * 0.29' as='int((nf+2)/2) * W/nf * 0.29'
+ pd='2*int((nf+1)/2) * (W/nf + 0.29)' ps='2*int((nf+2)/2) * (W/nf + 0.29)' nrd='0.29 / W' nrs='0.29 / W'
+ sa=0 sb=0 sd=0 mult=1 m=1
XM5 Vbn Vbn GND GND sky130_fd_pr__nfet_01v8 L=0.5 W=12 nf=1 ad='int((nf+1)/2) * W/nf * 0.29' as='int((nf+2)/2) * W/nf * 0.29'
+ pd='2*int((nf+1)/2) * (W/nf + 0.29)' ps='2*int((nf+2)/2) * (W/nf + 0.29)' nrd='0.29 / W' nrs='0.29 / W'
+ sa=0 sb=0 sd=0 mult=1 m=1
XM6 net4 net4 net3 GND sky130_fd_pr__nfet_01v8 L=0.5 W=48 nf=1 ad='int((nf+1)/2) * W/nf * 0.29' as='int((nf+2)/2) * W/nf * 0.29'
+ pd='2*int((nf+1)/2) * (W/nf + 0.29)' ps='2*int((nf+2)/2) * (W/nf + 0.29)' nrd='0.29 / W' nrs='0.29 / W'
+ sa=0 sb=0 sd=0 mult=1 m=1
XM7 Vcn Vcn net3 GND sky130_fd_pr__nfet_01v8 L=0.5 W=12 nf=1 ad='int((nf+1)/2) * W/nf * 0.29' as='int((nf+2)/2) * W/nf * 0.29'
+ pd='2*int((nf+1)/2) * (W/nf + 0.29)' ps='2*int((nf+2)/2) * (W/nf + 0.29)' nrd='0.29 / W' nrs='0.29 / W'
+ sa=0 sb=0 sd=0 mult=1 m=1
XM8 net1 net1 net2 VDD sky130_fd_pr__pfet_01v8 L=0.5 W=48 nf=1 ad='int((nf+1)/2) * W/nf * 0.29' as='int((nf+2)/2) * W/nf * 0.29'
+ pd='2*int((nf+1)/2) * (W/nf + 0.29)' ps='2*int((nf+2)/2) * (W/nf + 0.29)' nrd='0.29 / W' nrs='0.29 / W'
+ sa=0 sb=0 sd=0 mult=1 m=1
XM9 net2 net1 VDD VDD sky130_fd_pr__pfet_01v8 L=0.5 W=12 nf=1 ad='int((nf+1)/2) * W/nf * 0.29' as='int((nf+2)/2) * W/nf * 0.29'
+ pd='2*int((nf+1)/2) * (W/nf + 0.29)' ps='2*int((nf+2)/2) * (W/nf + 0.29)' nrd='0.29 / W' nrs='0.29 / W'
+ sa=0 sb=0 sd=0 mult=1 m=1
XM10 Vcp Vcp net2 VDD sky130_fd_pr__pfet_01v8 L=0.5 W=12 nf=1 ad='int((nf+1)/2) * W/nf * 0.29' as='int((nf+2)/2) * W/nf * 0.29'
+ pd='2*int((nf+1)/2) * (W/nf + 0.29)' ps='2*int((nf+2)/2) * (W/nf + 0.29)' nrd='0.29 / W' nrs='0.29 / W'
+ sa=0 sb=0 sd=0 mult=1 m=1
XM11 Vbp Vbp VDD VDD sky130_fd_pr__pfet_01v8 L=0.5 W=12 nf=1 ad='int((nf+1)/2) * W/nf * 0.29' as='int((nf+2)/2) * W/nf * 0.29'
+ pd='2*int((nf+1)/2) * (W/nf + 0.29)' ps='2*int((nf+2)/2) * (W/nf + 0.29)' nrd='0.29 / W' nrs='0.29 / W'
+ sa=0 sb=0 sd=0 mult=1 m=1
XM12 net4 Vbp VDD VDD sky130_fd_pr__pfet_01v8 L=2.5 W=12 nf=1 ad='int((nf+1)/2) * W/nf * 0.29' as='int((nf+2)/2) * W/nf * 0.29'
+ pd='2*int((nf+1)/2) * (W/nf + 0.29)' ps='2*int((nf+2)/2) * (W/nf + 0.29)' nrd='0.29 / W' nrs='0.29 / W'
+ sa=0 sb=0 sd=0 mult=1 m=1
XM13 Vcn Vbp VDD VDD sky130_fd_pr__pfet_01v8 L=0.5 W=12 nf=1 ad='int((nf+1)/2) * W/nf * 0.29' as='int((nf+2)/2) * W/nf * 0.29'
+ pd='2*int((nf+1)/2) * (W/nf + 0.29)' ps='2*int((nf+2)/2) * (W/nf + 0.29)' nrd='0.29 / W' nrs='0.29 / W'
+ sa=0 sb=0 sd=0 mult=1 m=1
I1 VDD Vbn 100u
.ends


* expanding   symbol:  ../schematics/digital_control.sym # of pins=22
** sym_path: schematics/digital_control.sym
** sch_path: schematics/digital_control.sch
.subckt digital_control STOn RCLn SH STOp RCLp SH_bar ENAD_bar PRE_bar PRE ENAD D D_bar CLK STOp_bar
+ STOn_bar RCLp_bar RCLn_bar D1 D2 D3 RST D_in
*.ipin D_in
*.opin D1
*.opin D2
*.opin D3
*.ipin CLK
*.opin SH_bar
*.opin SH
*.ipin PRE
*.opin PRE_bar
*.ipin ENAD
*.opin ENAD_bar
*.opin STOp
*.opin STOn
*.opin RCLp
*.opin RCLn
*.opin STOn_bar
*.opin STOp_bar
*.opin RCLn_bar
*.opin RCLp_bar
*.ipin RST
*.opin D
*.opin D_bar
x4 CLK_RST D2 D3 D2_bar D3_bar CRSL_edge_sens
x5 CLK_RST D1 D2 D1_bar D2_bar CRSL_edge_sens
x6 CLK_RST D D1 D_bar D1_bar CRSL_edge_sens
x10 VDD CLK STOn_bar D GND nand2
X13 STOn_bar STOn VDD GND inverter
X16 RCLn_bar RCLn VDD GND inverter
X17 STOp_bar STOp VDD GND inverter
X18 RCLp_bar RCLp VDD GND inverter
x19 VDD CLK RCLn_bar D_bar GND nand2
x20 VDD CLK STOp_bar D_bar GND nand2
x21 VDD CLK RCLp_bar D GND nand2
X23 D_in net1 VDD GND inverter
X12 CLK SH VDD GND inverter
X1 SH SH_bar VDD GND inverter
X11 PRE PRE_bar VDD GND inverter
X14 ENAD ENAD_bar VDD GND inverter
x2 CLK_RST D3 D_in D3_bar net1 CRSL_edge_sens
X7 SH CLK_RST RST nor2
.ends


* expanding   symbol:  ../schematics/CRSL_edge_sens.sym # of pins=5
** sym_path: schematics/CRSL_edge_sens.sym
** sch_path: schematics/CRSL_edge_sens.sch
.subckt CRSL_edge_sens Phi Q D Q_bar D_bar
*.ipin D
*.ipin D_bar
*.opin Q
*.opin Q_bar
*.ipin Phi
XM14 Q_bar Q GND GND sky130_fd_pr__nfet_01v8 L=0.15 W=1 nf=1 ad='int((nf+1)/2) * W/nf * 0.29' as='int((nf+2)/2) * W/nf * 0.29'
+ pd='2*int((nf+1)/2) * (W/nf + 0.29)' ps='2*int((nf+2)/2) * (W/nf + 0.29)' nrd='0.29 / W' nrs='0.29 / W'
+ sa=0 sb=0 sd=0 mult=1 m=1
XM2 Q_bar Phi net3 GND sky130_fd_pr__nfet_01v8 L=0.15 W=1 nf=1 ad='int((nf+1)/2) * W/nf * 0.29' as='int((nf+2)/2) * W/nf * 0.29'
+ pd='2*int((nf+1)/2) * (W/nf + 0.29)' ps='2*int((nf+2)/2) * (W/nf + 0.29)' nrd='0.29 / W' nrs='0.29 / W'
+ sa=0 sb=0 sd=0 mult=1 m=1
XM6 Q Phi net2 GND sky130_fd_pr__nfet_01v8 L=0.15 W=1 nf=1 ad='int((nf+1)/2) * W/nf * 0.29' as='int((nf+2)/2) * W/nf * 0.29'
+ pd='2*int((nf+1)/2) * (W/nf + 0.29)' ps='2*int((nf+2)/2) * (W/nf + 0.29)' nrd='0.29 / W' nrs='0.29 / W'
+ sa=0 sb=0 sd=0 mult=1 m=1
XM7 net4 Phi GND GND sky130_fd_pr__nfet_01v8 L=0.15 W=4 nf=1 ad='int((nf+1)/2) * W/nf * 0.29' as='int((nf+2)/2) * W/nf * 0.29'
+ pd='2*int((nf+1)/2) * (W/nf + 0.29)' ps='2*int((nf+2)/2) * (W/nf + 0.29)' nrd='0.29 / W' nrs='0.29 / W'
+ sa=0 sb=0 sd=0 mult=1 m=1
XM8 net3 net2 net4 GND sky130_fd_pr__nfet_01v8 L=0.15 W=1 nf=1 ad='int((nf+1)/2) * W/nf * 0.29' as='int((nf+2)/2) * W/nf * 0.29'
+ pd='2*int((nf+1)/2) * (W/nf + 0.29)' ps='2*int((nf+2)/2) * (W/nf + 0.29)' nrd='0.29 / W' nrs='0.29 / W'
+ sa=0 sb=0 sd=0 mult=1 m=1
XM12 net3 net2 VDD VDD sky130_fd_pr__pfet_01v8 L=0.15 W=1 nf=1 ad='int((nf+1)/2) * W/nf * 0.29' as='int((nf+2)/2) * W/nf * 0.29'
+ pd='2*int((nf+1)/2) * (W/nf + 0.29)' ps='2*int((nf+2)/2) * (W/nf + 0.29)' nrd='0.29 / W' nrs='0.29 / W'
+ sa=0 sb=0 sd=0 mult=1 m=1
XM9 net2 net3 VDD VDD sky130_fd_pr__pfet_01v8 L=0.15 W=1 nf=1 ad='int((nf+1)/2) * W/nf * 0.29' as='int((nf+2)/2) * W/nf * 0.29'
+ pd='2*int((nf+1)/2) * (W/nf + 0.29)' ps='2*int((nf+2)/2) * (W/nf + 0.29)' nrd='0.29 / W' nrs='0.29 / W'
+ sa=0 sb=0 sd=0 mult=1 m=1
XM1 net1 Phi VDD VDD sky130_fd_pr__pfet_01v8 L=0.15 W=4 nf=1 ad='int((nf+1)/2) * W/nf * 0.29' as='int((nf+2)/2) * W/nf * 0.29'
+ pd='2*int((nf+1)/2) * (W/nf + 0.29)' ps='2*int((nf+2)/2) * (W/nf + 0.29)' nrd='0.29 / W' nrs='0.29 / W'
+ sa=0 sb=0 sd=0 mult=1 m=1
XM3 Q_bar Q net1 VDD sky130_fd_pr__pfet_01v8 L=0.15 W=1 nf=1 ad='int((nf+1)/2) * W/nf * 0.29' as='int((nf+2)/2) * W/nf * 0.29'
+ pd='2*int((nf+1)/2) * (W/nf + 0.29)' ps='2*int((nf+2)/2) * (W/nf + 0.29)' nrd='0.29 / W' nrs='0.29 / W'
+ sa=0 sb=0 sd=0 mult=1 m=1
XM4 Q Q_bar net1 VDD sky130_fd_pr__pfet_01v8 L=0.15 W=1 nf=1 ad='int((nf+1)/2) * W/nf * 0.29' as='int((nf+2)/2) * W/nf * 0.29'
+ pd='2*int((nf+1)/2) * (W/nf + 0.29)' ps='2*int((nf+2)/2) * (W/nf + 0.29)' nrd='0.29 / W' nrs='0.29 / W'
+ sa=0 sb=0 sd=0 mult=1 m=1
XM10 Q Q_bar GND GND sky130_fd_pr__nfet_01v8 L=0.15 W=1 nf=1 ad='int((nf+1)/2) * W/nf * 0.29' as='int((nf+2)/2) * W/nf * 0.29'
+ pd='2*int((nf+1)/2) * (W/nf + 0.29)' ps='2*int((nf+2)/2) * (W/nf + 0.29)' nrd='0.29 / W' nrs='0.29 / W'
+ sa=0 sb=0 sd=0 mult=1 m=1
XM5 net2 net3 net4 GND sky130_fd_pr__nfet_01v8 L=0.15 W=1 nf=1 ad='int((nf+1)/2) * W/nf * 0.29' as='int((nf+2)/2) * W/nf * 0.29'
+ pd='2*int((nf+1)/2) * (W/nf + 0.29)' ps='2*int((nf+2)/2) * (W/nf + 0.29)' nrd='0.29 / W' nrs='0.29 / W'
+ sa=0 sb=0 sd=0 mult=1 m=1
XM11 net3 Phi D_bar VDD sky130_fd_pr__pfet_01v8 L=0.15 W=1 nf=1 ad='int((nf+1)/2) * W/nf * 0.29' as='int((nf+2)/2) * W/nf * 0.29'
+ pd='2*int((nf+1)/2) * (W/nf + 0.29)' ps='2*int((nf+2)/2) * (W/nf + 0.29)' nrd='0.29 / W' nrs='0.29 / W'
+ sa=0 sb=0 sd=0 mult=1 m=1
XM15 net2 Phi D VDD sky130_fd_pr__pfet_01v8 L=0.15 W=1 nf=1 ad='int((nf+1)/2) * W/nf * 0.29' as='int((nf+2)/2) * W/nf * 0.29'
+ pd='2*int((nf+1)/2) * (W/nf + 0.29)' ps='2*int((nf+2)/2) * (W/nf + 0.29)' nrd='0.29 / W' nrs='0.29 / W'
+ sa=0 sb=0 sd=0 mult=1 m=1
.ends


* expanding   symbol:  ../schematics/nand2.sym # of pins=5
** sym_path: schematics/nand2.sym
** sch_path: schematics/nand2.sch
.subckt nand2 VP B Y A VN
*.iopin VP
*.iopin VN
*.ipin A
*.ipin B
*.opin Y
XM5 Y B VP VP sky130_fd_pr__pfet_01v8 L=0.15 W=1 nf=1 ad='int((nf+1)/2) * W/nf * 0.29' as='int((nf+2)/2) * W/nf * 0.29'
+ pd='2*int((nf+1)/2) * (W/nf + 0.29)' ps='2*int((nf+2)/2) * (W/nf + 0.29)' nrd='0.29 / W' nrs='0.29 / W'
+ sa=0 sb=0 sd=0 mult=1 m=1
XM2 Y A VP VP sky130_fd_pr__pfet_01v8 L=0.15 W=1 nf=1 ad='int((nf+1)/2) * W/nf * 0.29' as='int((nf+2)/2) * W/nf * 0.29'
+ pd='2*int((nf+1)/2) * (W/nf + 0.29)' ps='2*int((nf+2)/2) * (W/nf + 0.29)' nrd='0.29 / W' nrs='0.29 / W'
+ sa=0 sb=0 sd=0 mult=1 m=1
XM1 Y A net1 VN sky130_fd_pr__nfet_01v8 L=0.15 W=1 nf=1 ad='int((nf+1)/2) * W/nf * 0.29' as='int((nf+2)/2) * W/nf * 0.29'
+ pd='2*int((nf+1)/2) * (W/nf + 0.29)' ps='2*int((nf+2)/2) * (W/nf + 0.29)' nrd='0.29 / W' nrs='0.29 / W'
+ sa=0 sb=0 sd=0 mult=1 m=1
XM3 net1 B VN VN sky130_fd_pr__nfet_01v8 L=0.15 W=1 nf=1 ad='int((nf+1)/2) * W/nf * 0.29' as='int((nf+2)/2) * W/nf * 0.29'
+ pd='2*int((nf+1)/2) * (W/nf + 0.29)' ps='2*int((nf+2)/2) * (W/nf + 0.29)' nrd='0.29 / W' nrs='0.29 / W'
+ sa=0 sb=0 sd=0 mult=1 m=1
.ends


* expanding   symbol:  ../schematics/inverter.sym # of pins=4
** sym_path: schematics/inverter.sym
** sch_path: schematics/inverter.sch
.subckt inverter A Y VP VN
*.ipin A
*.iopin VP
*.iopin VN
*.opin Y
XM1 Y A VP VDD sky130_fd_pr__pfet_01v8 L=0.15 W=1 nf=1 ad='int((nf+1)/2) * W/nf * 0.29' as='int((nf+2)/2) * W/nf * 0.29'
+ pd='2*int((nf+1)/2) * (W/nf + 0.29)' ps='2*int((nf+2)/2) * (W/nf + 0.29)' nrd='0.29 / W' nrs='0.29 / W'
+ sa=0 sb=0 sd=0 mult=1 m=1
XM2 Y A VN GND sky130_fd_pr__nfet_01v8 L=0.15 W=1 nf=1 ad='int((nf+1)/2) * W/nf * 0.29' as='int((nf+2)/2) * W/nf * 0.29'
+ pd='2*int((nf+1)/2) * (W/nf + 0.29)' ps='2*int((nf+2)/2) * (W/nf + 0.29)' nrd='0.29 / W' nrs='0.29 / W'
+ sa=0 sb=0 sd=0 mult=1 m=1
.ends


* expanding   symbol:  /home/madvlsi/Documents/algorithmic-ada-converter/schematics/nor2.sym # of
*+ pins=3
** sym_path: schematics/nor2.sym
** sch_path: schematics/nor2.sch
.subckt nor2 A Y B
*.ipin A
*.ipin B
*.opin Y
XM4 Y B GND GND sky130_fd_pr__nfet_01v8 L=0.15 W=1 nf=1 ad='int((nf+1)/2) * W/nf * 0.29' as='int((nf+2)/2) * W/nf * 0.29'
+ pd='2*int((nf+1)/2) * (W/nf + 0.29)' ps='2*int((nf+2)/2) * (W/nf + 0.29)' nrd='0.29 / W' nrs='0.29 / W'
+ sa=0 sb=0 sd=0 mult=1 m=1
XM6 Y A GND GND sky130_fd_pr__nfet_01v8 L=0.15 W=1 nf=1 ad='int((nf+1)/2) * W/nf * 0.29' as='int((nf+2)/2) * W/nf * 0.29'
+ pd='2*int((nf+1)/2) * (W/nf + 0.29)' ps='2*int((nf+2)/2) * (W/nf + 0.29)' nrd='0.29 / W' nrs='0.29 / W'
+ sa=0 sb=0 sd=0 mult=1 m=1
XM7 Y B net1 VDD sky130_fd_pr__pfet_01v8 L=0.15 W=1 nf=1 ad='int((nf+1)/2) * W/nf * 0.29' as='int((nf+2)/2) * W/nf * 0.29'
+ pd='2*int((nf+1)/2) * (W/nf + 0.29)' ps='2*int((nf+2)/2) * (W/nf + 0.29)' nrd='0.29 / W' nrs='0.29 / W'
+ sa=0 sb=0 sd=0 mult=1 m=1
XM8 net1 A VDD VDD sky130_fd_pr__pfet_01v8 L=0.15 W=1 nf=1 ad='int((nf+1)/2) * W/nf * 0.29' as='int((nf+2)/2) * W/nf * 0.29'
+ pd='2*int((nf+1)/2) * (W/nf + 0.29)' ps='2*int((nf+2)/2) * (W/nf + 0.29)' nrd='0.29 / W' nrs='0.29 / W'
+ sa=0 sb=0 sd=0 mult=1 m=1
.ends

.GLOBAL GND
.GLOBAL VDD
.end
